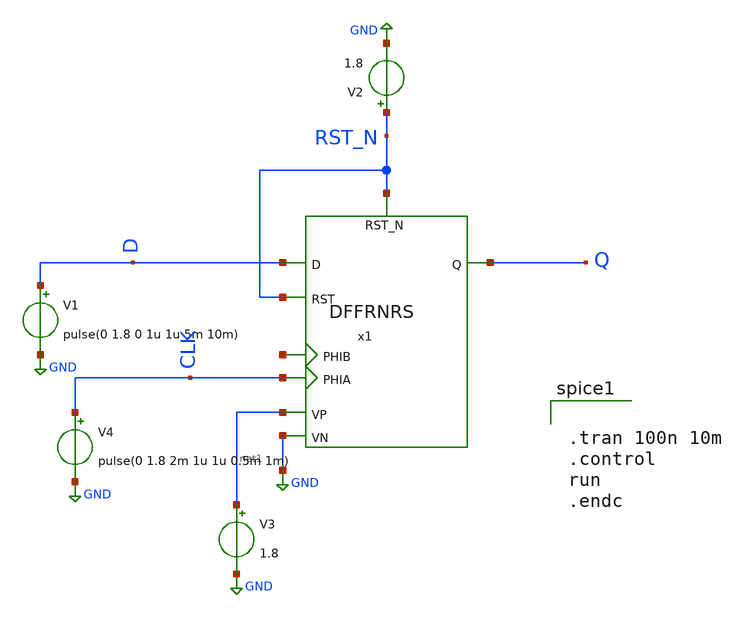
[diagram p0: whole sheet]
** sch_path: ADC/4bit_C2C/MagicAndSpice/EE431_FinalProj/DFFRNRS_tb.sch
**.subckt DFFRNRS_tb
V2 RST_N GND 1.8
V3 net1 GND 1.8
V4 CLK GND pulse(0 1.8 2m 1u 1u 0.5m 1m)
V1 D GND pulse(0 1.8 0 1u 1u 5m 10m)
x1 CLK net2 D Q RST_N RST_N net1 GND DFFRNRS
**** begin user architecture code
 .lib $::SKYWATER_MODELS/sky130.lib.spice tt


.tran 100n 10m
.control
run
.endc

**** end user architecture code
**.ends
.GLOBAL GND
.end
